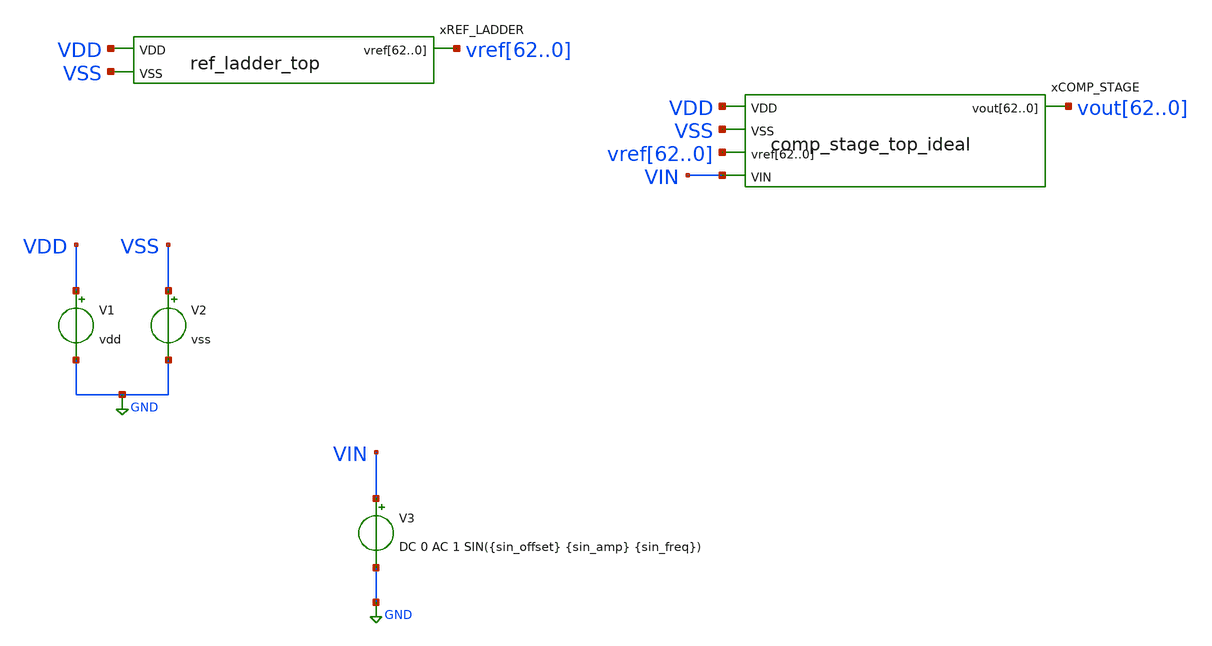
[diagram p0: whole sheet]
** sch_path: simulation/tb_comp_stage_top.sch
**.subckt tb_comp_stage_top
V1 VDD GND vdd
V2 VSS GND vss
V3 VIN GND DC 0 AC 1 SIN({sin_offset} {sin_amp} {sin_freq})
xCOMP_STAGE vout62 vout61 vout60 vout59 vout58 vout57 vout56 vout55 vout54 vout53 vout52 vout51
+ vout50 vout49 vout48 vout47 vout46 vout45 vout44 vout43 vout42 vout41 vout40 vout39 vout38 vout37 vout36
+ vout35 vout34 vout33 vout32 vout31 vout30 vout29 vout28 vout27 vout26 vout25 vout24 vout23 vout22 vout21
+ vout20 vout19 vout18 vout17 vout16 vout15 vout14 vout13 vout12 vout11 vout10 vout9 vout8 vout7 vout6 vout5
+ vout4 vout3 vout2 vout1 vout0 VDD VSS vref62 vref61 vref60 vref59 vref58 vref57 vref56 vref55 vref54
+ vref53 vref52 vref51 vref50 vref49 vref48 vref47 vref46 vref45 vref44 vref43 vref42 vref41 vref40 vref39
+ vref38 vref37 vref36 vref35 vref34 vref33 vref32 vref31 vref30 vref29 vref28 vref27 vref26 vref25 vref24
+ vref23 vref22 vref21 vref20 vref19 vref18 vref17 vref16 vref15 vref14 vref13 vref12 vref11 vref10 vref9
+ vref8 vref7 vref6 vref5 vref4 vref3 vref2 vref1 vref0 VIN comp_stage_top_ideal
xREF_LADDER VDD vref62 vref61 vref60 vref59 vref58 vref57 vref56 vref55 vref54 vref53 vref52 vref51
+ vref50 vref49 vref48 vref47 vref46 vref45 vref44 vref43 vref42 vref41 vref40 vref39 vref38 vref37 vref36
+ vref35 vref34 vref33 vref32 vref31 vref30 vref29 vref28 vref27 vref26 vref25 vref24 vref23 vref22 vref21
+ vref20 vref19 vref18 vref17 vref16 vref15 vref14 vref13 vref12 vref11 vref10 vref9 vref8 vref7 vref6 vref5
+ vref4 vref3 vref2 vref1 vref0 VSS ref_ladder_top
**** begin user architecture code



# Model files
.lib /usr/local/share/pdk/sky130A/libs.tech/ngspice/sky130.lib.spice tt

# Main parameters
.param vdd=1.8 vss=0 vhigh=1.8 vlow=0
.param sin_offset='vdd/2'
.param sin_amp='vdd/2'
.param sin_freq=10Meg
.param sin_period='1/sin_freq'
.param tran_step='sin_period/10'
.param tran_stop_time='sin_period*2'

# Component parameters



# Save settings
.save all


# Analysis
.op
.tran {tran_step} {tran_stop_time}

# Start control block
.control

# Run sim
run

# Expressions

# Save expressions

# Write to raw file
write tb_comp_stage_top.raw
# wrdata custom_output.txt



.endc



**** end user architecture code
**.ends
.GLOBAL GND
.end
